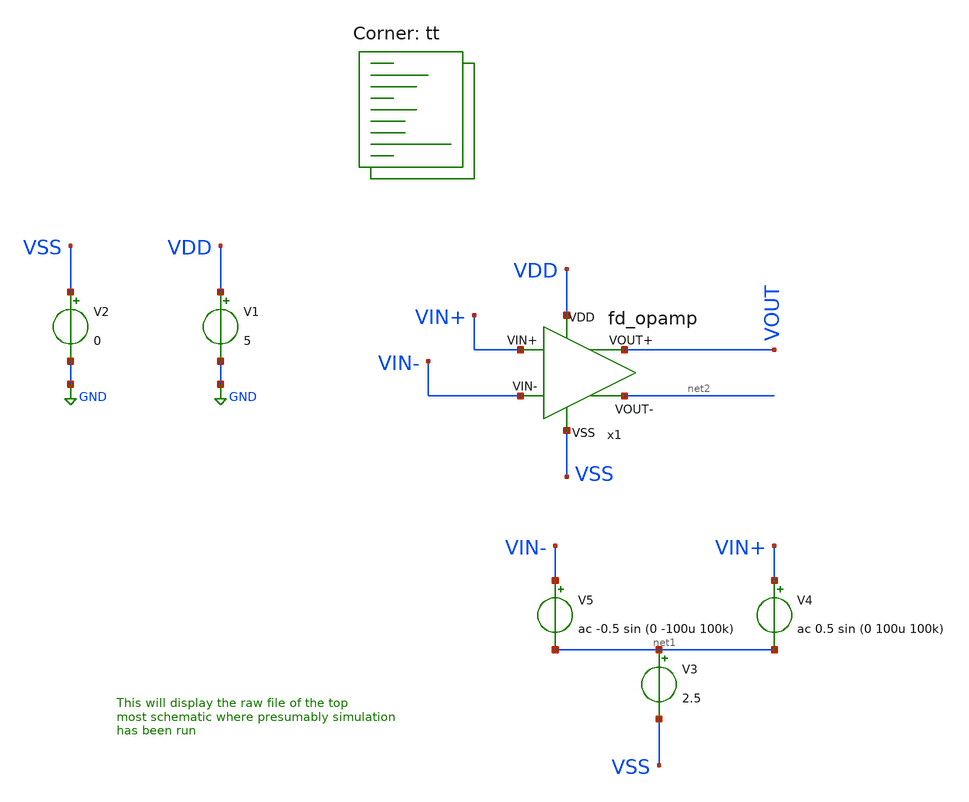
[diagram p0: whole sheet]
** sch_path: my_ip/sky130A/fully_differential_telescopic_cascode_5V_V1/tb/tb.sch
**.subckt tb
V1 VDD GND 5
V2 VSS GND 0
x1 VDD VSS VIN+ VOUT VIN- net2 fd_opamp
V3 net1 VSS 2.5
V4 VIN+ net1 ac 0.5 sin (0 100u 100k)
V5 VIN- net1 ac -0.5 sin (0 -100u 100k)
**** begin user architecture code
.lib $::SKYWATER_MODELS/sky130.lib.spice tt
**** end user architecture code
**.ends
.GLOBAL GND
**** begin user architecture code


* ngspice commands
.options savecurrents
.TEMP 27
.control
save all
save @m.x1.xm1.msky130_fd_pr__pfet_g5v0d10v5[gm]
save @m.x1.xm1.msky130_fd_pr__pfet_g5v0d10v5[vth]
save @m.x1.xm1.msky130_fd_pr__pfet_g5v0d10v5[vds]
save @m.x1.xm1.msky130_fd_pr__pfet_g5v0d10v5[vgs]

save @m.x1.xm2.msky130_fd_pr__pfet_g5v0d10v5[gm]
save @m.x1.xm2.msky130_fd_pr__pfet_g5v0d10v5[vth]
save @m.x1.xm2.msky130_fd_pr__pfet_g5v0d10v5[vds]
save @m.x1.xm2.msky130_fd_pr__pfet_g5v0d10v5[vgs]

save @m.x1.xm3.msky130_fd_pr__pfet_g5v0d10v5[gm]
save @m.x1.xm3.msky130_fd_pr__pfet_g5v0d10v5[vth]
save @m.x1.xm3.msky130_fd_pr__pfet_g5v0d10v5[vds]
save @m.x1.xm3.msky130_fd_pr__pfet_g5v0d10v5[vgs]

save @m.x1.xm4.msky130_fd_pr__pfet_g5v0d10v5[gm]
save @m.x1.xm4.msky130_fd_pr__pfet_g5v0d10v5[vth]
save @m.x1.xm4.msky130_fd_pr__pfet_g5v0d10v5[vds]
save @m.x1.xm4.msky130_fd_pr__pfet_g5v0d10v5[vgs]

save @m.x1.xm5.msky130_fd_pr__nfet_g5v0d10v5[gm]
save @m.x1.xm5.msky130_fd_pr__nfet_g5v0d10v5[vth]
save @m.x1.xm5.msky130_fd_pr__nfet_g5v0d10v5[vds]
save @m.x1.xm5.msky130_fd_pr__nfet_g5v0d10v5[vgs]

save @m.x1.xm6.msky130_fd_pr__nfet_g5v0d10v5[gm]
save @m.x1.xm6.msky130_fd_pr__nfet_g5v0d10v5[vth]
save @m.x1.xm6.msky130_fd_pr__nfet_g5v0d10v5[vds]
save @m.x1.xm6.msky130_fd_pr__nfet_g5v0d10v5[vgs]

save @m.x1.xm7.msky130_fd_pr__nfet_g5v0d10v5[gm]
save @m.x1.xm7.msky130_fd_pr__nfet_g5v0d10v5[vth]
save @m.x1.xm7.msky130_fd_pr__nfet_g5v0d10v5[vds]
save @m.x1.xm7.msky130_fd_pr__nfet_g5v0d10v5[vgs]

save @m.x1.xm8.msky130_fd_pr__nfet_g5v0d10v5[gm]
save @m.x1.xm8.msky130_fd_pr__nfet_g5v0d10v5[vth]
save @m.x1.xm8.msky130_fd_pr__nfet_g5v0d10v5[vds]
save @m.x1.xm8.msky130_fd_pr__nfet_g5v0d10v5[vgs]

save @m.x1.xm9.msky130_fd_pr__pfet_g5v0d10v5[gm]
save @m.x1.xm9.msky130_fd_pr__pfet_g5v0d10v5[vth]
save @m.x1.xm9.msky130_fd_pr__pfet_g5v0d10v5[vds]
save @m.x1.xm9.msky130_fd_pr__pfet_g5v0d10v5[vgs]

save @m.x1.xm10.msky130_fd_pr__pfet_g5v0d10v5[gm]
save @m.x1.xm10.msky130_fd_pr__pfet_g5v0d10v5[vth]
save @m.x1.xm10.msky130_fd_pr__pfet_g5v0d10v5[vds]
save @m.x1.xm10.msky130_fd_pr__pfet_g5v0d10v5[vgs]

save @m.x1.xm11.msky130_fd_pr__pfet_g5v0d10v5[gm]
save @m.x1.xm11.msky130_fd_pr__pfet_g5v0d10v5[vth]
save @m.x1.xm11.msky130_fd_pr__pfet_g5v0d10v5[vds]
save @m.x1.xm11.msky130_fd_pr__pfet_g5v0d10v5[vgs]

save @m.x1.xm12.msky130_fd_pr__pfet_g5v0d10v5[gm]
save @m.x1.xm12.msky130_fd_pr__pfet_g5v0d10v5[vth]
save @m.x1.xm12.msky130_fd_pr__pfet_g5v0d10v5[vds]
save @m.x1.xm12.msky130_fd_pr__pfet_g5v0d10v5[vgs]

save @m.x1.xm13.msky130_fd_pr__nfet_g5v0d10v5[gm]
save @m.x1.xm13.msky130_fd_pr__nfet_g5v0d10v5[vth]
save @m.x1.xm13.msky130_fd_pr__nfet_g5v0d10v5[vds]
save @m.x1.xm13.msky130_fd_pr__nfet_g5v0d10v5[vgs]

save @m.x1.xm14.msky130_fd_pr__nfet_g5v0d10v5[gm]
save @m.x1.xm14.msky130_fd_pr__nfet_g5v0d10v5[vth]
save @m.x1.xm14.msky130_fd_pr__nfet_g5v0d10v5[vds]
save @m.x1.xm14.msky130_fd_pr__nfet_g5v0d10v5[vgs]

save @m.x1.xm15.msky130_fd_pr__nfet_g5v0d10v5[gm]
save @m.x1.xm15.msky130_fd_pr__nfet_g5v0d10v5[vth]
save @m.x1.xm15.msky130_fd_pr__nfet_g5v0d10v5[vds]
save @m.x1.xm15.msky130_fd_pr__nfet_g5v0d10v5[vgs]

save @m.x1.xm16.msky130_fd_pr__nfet_g5v0d10v5[gm]
save @m.x1.xm16.msky130_fd_pr__nfet_g5v0d10v5[vth]
save @m.x1.xm16.msky130_fd_pr__nfet_g5v0d10v5[vds]
save @m.x1.xm16.msky130_fd_pr__nfet_g5v0d10v5[vgs]


save @m.x1.xm17.msky130_fd_pr__pfet_g5v0d10v5[gm]
save @m.x1.xm17.msky130_fd_pr__pfet_g5v0d10v5[vth]
save @m.x1.xm17.msky130_fd_pr__pfet_g5v0d10v5[vds]
save @m.x1.xm17.msky130_fd_pr__pfet_g5v0d10v5[vgs]

save @m.x1.xm18.msky130_fd_pr__pfet_g5v0d10v5[gm]
save @m.x1.xm18.msky130_fd_pr__pfet_g5v0d10v5[vth]
save @m.x1.xm18.msky130_fd_pr__pfet_g5v0d10v5[vds]
save @m.x1.xm18.msky130_fd_pr__pfet_g5v0d10v5[vgs]

save @m.x1.xm19.msky130_fd_pr__pfet_g5v0d10v5[gm]
save @m.x1.xm19.msky130_fd_pr__pfet_g5v0d10v5[vth]
save @m.x1.xm19.msky130_fd_pr__pfet_g5v0d10v5[vds]
save @m.x1.xm19.msky130_fd_pr__pfet_g5v0d10v5[vgs]

save @m.x1.xm20.msky130_fd_pr__pfet_g5v0d10v5[gm]
save @m.x1.xm20.msky130_fd_pr__pfet_g5v0d10v5[vth]
save @m.x1.xm20.msky130_fd_pr__pfet_g5v0d10v5[vds]
save @m.x1.xm20.msky130_fd_pr__pfet_g5v0d10v5[vgs]

save @m.x1.xm21.msky130_fd_pr__pfet_g5v0d10v5[gm]
save @m.x1.xm21.msky130_fd_pr__pfet_g5v0d10v5[vth]
save @m.x1.xm21.msky130_fd_pr__pfet_g5v0d10v5[vds]
save @m.x1.xm21.msky130_fd_pr__pfet_g5v0d10v5[vgs]

save @m.x1.xm22.msky130_fd_pr__pfet_g5v0d10v5[gm]
save @m.x1.xm22.msky130_fd_pr__pfet_g5v0d10v5[vth]
save @m.x1.xm22.msky130_fd_pr__pfet_g5v0d10v5[vds]
save @m.x1.xm22.msky130_fd_pr__pfet_g5v0d10v5[vgs]

save @m.x1.xm23.msky130_fd_pr__nfet_g5v0d10v5[gm]
save @m.x1.xm23.msky130_fd_pr__nfet_g5v0d10v5[vth]
save @m.x1.xm23.msky130_fd_pr__nfet_g5v0d10v5[vds]
save @m.x1.xm23.msky130_fd_pr__nfet_g5v0d10v5[vgs]

save @m.x1.xm24.msky130_fd_pr__nfet_g5v0d10v5[gm]
save @m.x1.xm24.msky130_fd_pr__nfet_g5v0d10v5[vth]
save @m.x1.xm24.msky130_fd_pr__nfet_g5v0d10v5[vds]
save @m.x1.xm24.msky130_fd_pr__nfet_g5v0d10v5[vgs]

op
write tb.raw

ac dec 10 1 50G
plot db(v(VOUT)) (180*ph(v(VOUT))/pi)
set appendwrite
write tb.raw

tran 1ns 30u
plot v(VOUT)
set appendwrite
write tb.raw
.endc



**** end user architecture code
.end
